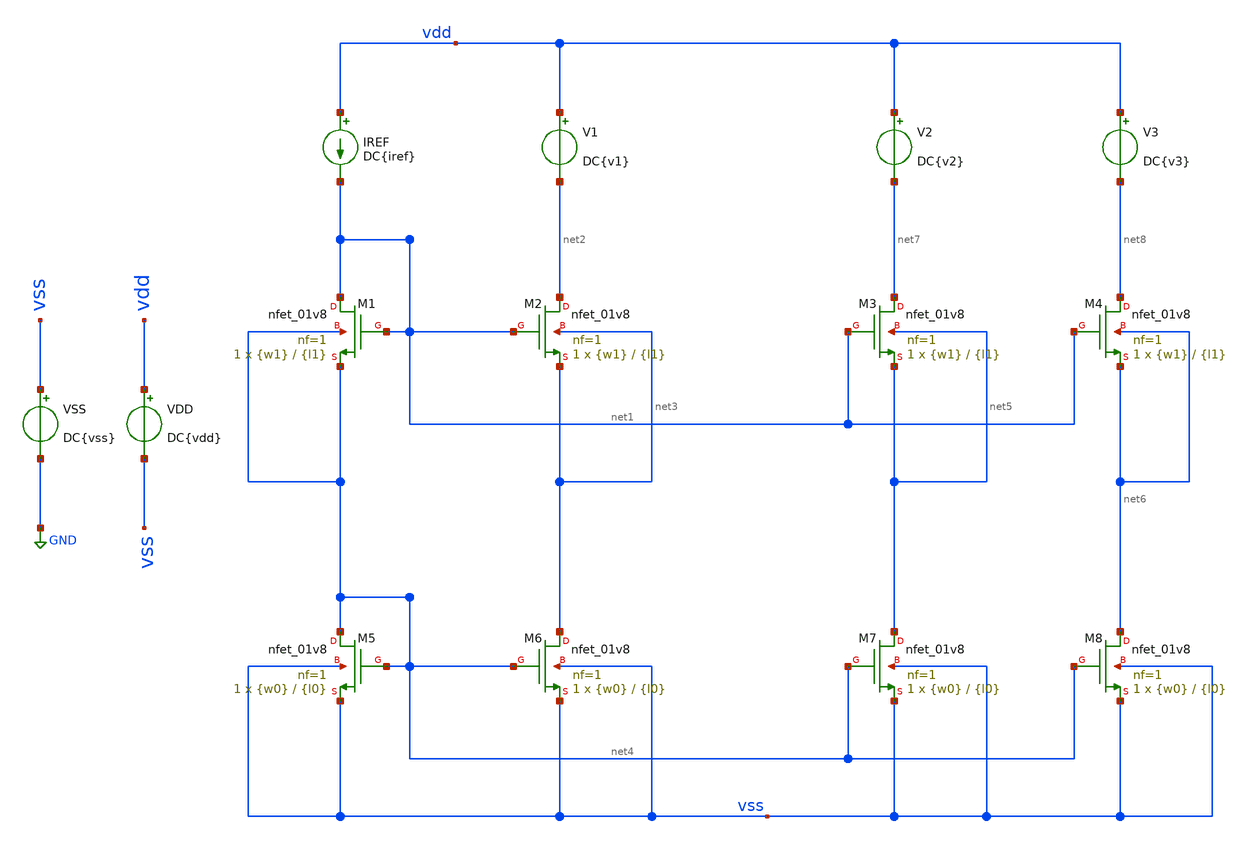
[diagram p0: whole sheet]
** sch_path: Tp2/Mis Simulaciones/tp2_3a.sch
**.subckt tp2_3a
XM1 net1 net1 net4 net4 sky130_fd_pr__nfet_01v8 L={l1} W={w1} nf=1 ad='int((nf+1)/2) * W/nf * 0.29' as='int((nf+2)/2) * W/nf * 0.29'
+ pd='2*int((nf+1)/2) * (W/nf + 0.29)' ps='2*int((nf+2)/2) * (W/nf + 0.29)' nrd='0.29 / W' nrs='0.29 / W'
+ sa=0 sb=0 sd=0 mult=1 m=1
XM2 net2 net1 net3 net3 sky130_fd_pr__nfet_01v8 L={l1} W={w1} nf=1 ad='int((nf+1)/2) * W/nf * 0.29' as='int((nf+2)/2) * W/nf * 0.29'
+ pd='2*int((nf+1)/2) * (W/nf + 0.29)' ps='2*int((nf+2)/2) * (W/nf + 0.29)' nrd='0.29 / W' nrs='0.29 / W'
+ sa=0 sb=0 sd=0 mult=1 m=1
IREF vdd net1 DC{iref}
VSS vss GND DC{vss}
VDD vdd vss DC{vdd}
XM3 net7 net1 net5 net5 sky130_fd_pr__nfet_01v8 L={l1} W={w1} nf=1 ad='int((nf+1)/2) * W/nf * 0.29' as='int((nf+2)/2) * W/nf * 0.29'
+ pd='2*int((nf+1)/2) * (W/nf + 0.29)' ps='2*int((nf+2)/2) * (W/nf + 0.29)' nrd='0.29 / W' nrs='0.29 / W'
+ sa=0 sb=0 sd=0 mult=1 m=1
XM4 net8 net1 net6 net6 sky130_fd_pr__nfet_01v8 L={l1} W={w1} nf=1 ad='int((nf+1)/2) * W/nf * 0.29' as='int((nf+2)/2) * W/nf * 0.29'
+ pd='2*int((nf+1)/2) * (W/nf + 0.29)' ps='2*int((nf+2)/2) * (W/nf + 0.29)' nrd='0.29 / W' nrs='0.29 / W'
+ sa=0 sb=0 sd=0 mult=1 m=1
V2 vdd net7 DC{v2}
V3 vdd net8 DC{v3}
V1 vdd net2 DC{v1}
XM5 net4 net4 vss vss sky130_fd_pr__nfet_01v8 L={l0} W={w0} nf=1 ad='int((nf+1)/2) * W/nf * 0.29' as='int((nf+2)/2) * W/nf * 0.29'
+ pd='2*int((nf+1)/2) * (W/nf + 0.29)' ps='2*int((nf+2)/2) * (W/nf + 0.29)' nrd='0.29 / W' nrs='0.29 / W'
+ sa=0 sb=0 sd=0 mult=1 m=1
XM6 net3 net4 vss vss sky130_fd_pr__nfet_01v8 L={l0} W={w0} nf=1 ad='int((nf+1)/2) * W/nf * 0.29' as='int((nf+2)/2) * W/nf * 0.29'
+ pd='2*int((nf+1)/2) * (W/nf + 0.29)' ps='2*int((nf+2)/2) * (W/nf + 0.29)' nrd='0.29 / W' nrs='0.29 / W'
+ sa=0 sb=0 sd=0 mult=1 m=1
XM7 net5 net4 vss vss sky130_fd_pr__nfet_01v8 L={l0} W={w0} nf=1 ad='int((nf+1)/2) * W/nf * 0.29' as='int((nf+2)/2) * W/nf * 0.29'
+ pd='2*int((nf+1)/2) * (W/nf + 0.29)' ps='2*int((nf+2)/2) * (W/nf + 0.29)' nrd='0.29 / W' nrs='0.29 / W'
+ sa=0 sb=0 sd=0 mult=1 m=1
XM8 net6 net4 vss vss sky130_fd_pr__nfet_01v8 L={l0} W={w0} nf=1 ad='int((nf+1)/2) * W/nf * 0.29' as='int((nf+2)/2) * W/nf * 0.29'
+ pd='2*int((nf+1)/2) * (W/nf + 0.29)' ps='2*int((nf+2)/2) * (W/nf + 0.29)' nrd='0.29 / W' nrs='0.29 / W'
+ sa=0 sb=0 sd=0 mult=1 m=1
**** begin user architecture code



* Parameters
.param vdd = 1.8
.param vss = 0.0
.param iref = 200u
.param w0 = 3.4
.param l0 = 0.9
.param w1 = 8.4
.param l1 = 0.15
.param v1 = 0.6
.param v2 = 0.9
.param v3 = 1.2
.options TEMPS = 27.0

* Models
.lib ~/skywater/skywater-pdk/libraries/sky130_fd_pr_ngspice/latest/models/corners/sky130.lib TT

* Data to save
.save all  @M.XM1.msky130_fd_pr__nfet_01v8[id]  @M.XM1.msky130_fd_pr__nfet_01v8[vth]  @M.XM1.msky130_fd_pr__nfet_01v8[vdsat]  @M.XM1.msky130_fd_pr__nfet_01v8[gm]  @M.XM1.msky130_fd_pr__nfet_01v8[vds]  @M.XM1.msky130_fd_pr__nfet_01v8[vgs]  @M.XM1.msky130_fd_pr__nfet_01v8[w]  @M.XM2.msky130_fd_pr__nfet_01v8[id]  @M.XM2.msky130_fd_pr__nfet_01v8[vth]  @M.XM2.msky130_fd_pr__nfet_01v8[vdsat]  @M.XM2.msky130_fd_pr__nfet_01v8[gm]  @M.XM2.msky130_fd_pr__nfet_01v8[vds]  @M.XM2.msky130_fd_pr__nfet_01v8[vgs]  @M.XM2.msky130_fd_pr__nfet_01v8[w]  @M.XM3.msky130_fd_pr__nfet_01v8[id]  @M.XM3.msky130_fd_pr__nfet_01v8[vth]  @M.XM3.msky130_fd_pr__nfet_01v8[vdsat]  @M.XM3.msky130_fd_pr__nfet_01v8[gm]  @M.XM3.msky130_fd_pr__nfet_01v8[vds]  @M.XM3.msky130_fd_pr__nfet_01v8[vgs]  @M.XM3.msky130_fd_pr__nfet_01v8[w]  @M.XM4.msky130_fd_pr__nfet_01v8[id]  @M.XM4.msky130_fd_pr__nfet_01v8[vth]  @M.XM4.msky130_fd_pr__nfet_01v8[vdsat]  @M.XM4.msky130_fd_pr__nfet_01v8[gm]  @M.XM4.msky130_fd_pr__nfet_01v8[vds]  @M.XM4.msky130_fd_pr__nfet_01v8[vgs]  @M.XM4.msky130_fd_pr__nfet_01v8[w]  @M.XM5.msky130_fd_pr__nfet_01v8[id]  @M.XM5.msky130_fd_pr__nfet_01v8[vth]  @M.XM5.msky130_fd_pr__nfet_01v8[vdsat]  @M.XM5.msky130_fd_pr__nfet_01v8[gm]  @M.XM5.msky130_fd_pr__nfet_01v8[vds]  @M.XM5.msky130_fd_pr__nfet_01v8[vgs]  @M.XM5.msky130_fd_pr__nfet_01v8[w]  @M.XM6.msky130_fd_pr__nfet_01v8[id]  @M.XM6.msky130_fd_pr__nfet_01v8[vth]  @M.XM6.msky130_fd_pr__nfet_01v8[vdsat]  @M.XM6.msky130_fd_pr__nfet_01v8[gm]  @M.XM6.msky130_fd_pr__nfet_01v8[vds]  @M.XM6.msky130_fd_pr__nfet_01v8[vgs]  @M.XM6.msky130_fd_pr__nfet_01v8[w]  @M.XM7.msky130_fd_pr__nfet_01v8[id]  @M.XM7.msky130_fd_pr__nfet_01v8[vth]  @M.XM7.msky130_fd_pr__nfet_01v8[vdsat]  @M.XM7.msky130_fd_pr__nfet_01v8[gm]  @M.XM7.msky130_fd_pr__nfet_01v8[vds]  @M.XM7.msky130_fd_pr__nfet_01v8[vgs]  @M.XM7.msky130_fd_pr__nfet_01v8[w]  @M.XM8.msky130_fd_pr__nfet_01v8[id]  @M.XM8.msky130_fd_pr__nfet_01v8[vth]  @M.XM8.msky130_fd_pr__nfet_01v8[vdsat]  @M.XM8.msky130_fd_pr__nfet_01v8[gm]  @M.XM8.msky130_fd_pr__nfet_01v8[vds]  @M.XM8.msky130_fd_pr__nfet_01v8[vgs]  @M.XM8.msky130_fd_pr__nfet_01v8[w]

* Simulation
.control
  *let wi = 1.5
  *let wf = 4.5
  *let wstep = 0.15

  *dowhile wi <= wf
    *print @M.XM1.msky130_fd_pr__nfet_01v8[w]
    *alter @M.XM1.msky130_fd_pr__nfet_01v8[w] = wi
    *alter @M.XM2.msky130_fd_pr__nfet_01v8[w] = wi
    *let wi = wi + wstep
    *op
    *print @M.XM1.msky130_fd_pr__nfet_01v8[w]
    *print @M.XM1.msky130_fd_pr__nfet_01v8[id]
    *print @M.XM1.msky130_fd_pr__nfet_01v8[vds]
    *print @M.XM1.msky130_fd_pr__nfet_01v8[vgs]
    *print @M.XM2.msky130_fd_pr__nfet_01v8[w]
    *print @M.XM2.msky130_fd_pr__nfet_01v8[id]
    *print @M.XM2.msky130_fd_pr__nfet_01v8[vds]
    *print @M.XM2.msky130_fd_pr__nfet_01v8[vgs]
    *print @M.XM3.msky130_fd_pr__nfet_01v8[w]
    *print @M.XM3.msky130_fd_pr__nfet_01v8[id]
    *print @M.XM3.msky130_fd_pr__nfet_01v8[vds]
    *print @M.XM3.msky130_fd_pr__nfet_01v8[vgs]
    *print @M.XM4.msky130_fd_pr__nfet_01v8[w]
    *print @M.XM4.msky130_fd_pr__nfet_01v8[id]
    *print @M.XM4.msky130_fd_pr__nfet_01v8[vds]
    *print @M.XM4.msky130_fd_pr__nfet_01v8[vgs]
    *print @M.XM5.msky130_fd_pr__nfet_01v8[w]
    *print @M.XM5.msky130_fd_pr__nfet_01v8[id]
    *print @M.XM5.msky130_fd_pr__nfet_01v8[vds]
    *print @M.XM5.msky130_fd_pr__nfet_01v8[vgs]
    *print @M.XM6.msky130_fd_pr__nfet_01v8[w]
    *print @M.XM6.msky130_fd_pr__nfet_01v8[id]
    *print @M.XM6.msky130_fd_pr__nfet_01v8[vds]
    *print @M.XM6.msky130_fd_pr__nfet_01v8[vgs]
    *print @M.XM7.msky130_fd_pr__nfet_01v8[w]
    *print @M.XM7.msky130_fd_pr__nfet_01v8[id]
    *print @M.XM7.msky130_fd_pr__nfet_01v8[vds]
    *print @M.XM7.msky130_fd_pr__nfet_01v8[vgs]
    *print @M.XM8.msky130_fd_pr__nfet_01v8[w]
    *print @M.XM8.msky130_fd_pr__nfet_01v8[id]
    *print @M.XM8.msky130_fd_pr__nfet_01v8[vds]
    *print @M.XM8.msky130_fd_pr__nfet_01v8[vgs]
    *save all
  *end
  *write tp2_3a.raw

  unset filetype
  op
  save all
  write tp2_3a.raw

.endc

.end


**** end user architecture code
**.ends
.GLOBAL GND
.end
